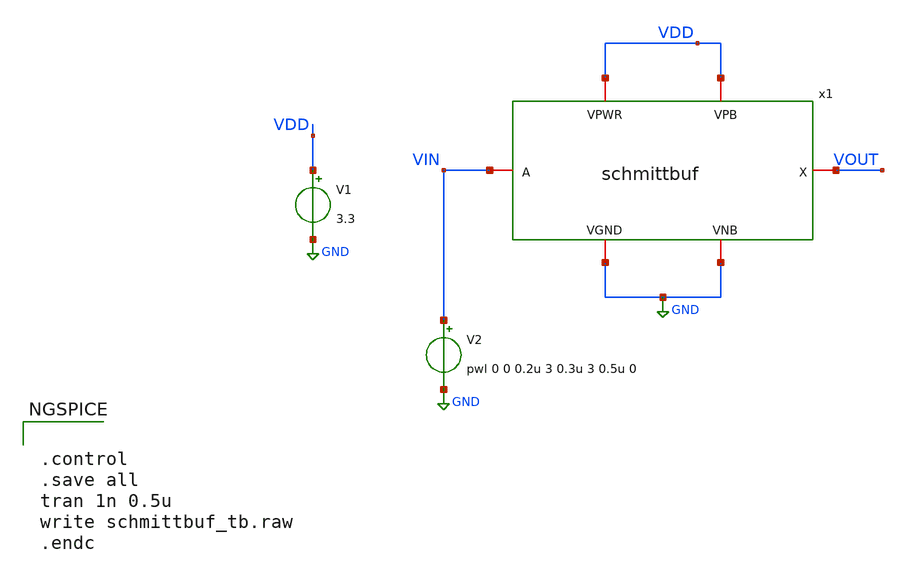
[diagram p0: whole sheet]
** sch_path: images/iic-osic-tools/addons/examples/open-pmic/design/oscillator/schmittbuf_tb.sch
**.subckt schmittbuf_tb
x1 VDD GND VDD GND VIN VOUT schmittbuf
V1 VDD GND 3.3
V2 VIN GND pwl 0 0 0.2u 3 0.3u 3 0.5u 0
**** begin user architecture code

.include $::SKYWATER_MODELS/cells/nfet_01v8/sky130_fd_pr__nfet_01v8__tt.corner.spice
.include $::SKYWATER_MODELS/cells/nfet_01v8_lvt/sky130_fd_pr__nfet_01v8_lvt__tt.corner.spice
.include $::SKYWATER_MODELS/cells/pfet_01v8/sky130_fd_pr__pfet_01v8__tt.corner.spice
.include $::SKYWATER_MODELS/cells/nfet_03v3_nvt/sky130_fd_pr__nfet_03v3_nvt__tt.corner.spice
.include $::SKYWATER_MODELS/cells/nfet_05v0_nvt/sky130_fd_pr__nfet_05v0_nvt__tt.corner.spice
.include $::SKYWATER_MODELS/cells/esd_nfet_01v8/sky130_fd_pr__esd_nfet_01v8__tt.corner.spice
.include $::SKYWATER_MODELS/cells/pfet_01v8_lvt/sky130_fd_pr__pfet_01v8_lvt__tt.corner.spice
.include $::SKYWATER_MODELS/cells/pfet_01v8_hvt/sky130_fd_pr__pfet_01v8_hvt__tt.corner.spice
.include $::SKYWATER_MODELS/cells/esd_pfet_g5v0d10v5/sky130_fd_pr__esd_pfet_g5v0d10v5__tt.corner.spice
.include $::SKYWATER_MODELS/cells/pfet_g5v0d10v5/sky130_fd_pr__pfet_g5v0d10v5__tt.corner.spice
.include $::SKYWATER_MODELS/cells/pfet_g5v0d16v0/sky130_fd_pr__pfet_g5v0d16v0__tt.corner.spice
.include $::SKYWATER_MODELS/cells/nfet_g5v0d10v5/sky130_fd_pr__nfet_g5v0d10v5__tt.corner.spice
.include $::SKYWATER_MODELS/cells/nfet_g5v0d16v0/sky130_fd_pr__nfet_g5v0d16v0__tt_discrete.corner.spice
.include $::SKYWATER_MODELS/cells/esd_nfet_g5v0d10v5/sky130_fd_pr__esd_nfet_g5v0d10v5__tt.corner.spice
.include $::SKYWATER_MODELS/models/corners/tt/nonfet.spice
* Mismatch parameters
.include $::SKYWATER_MODELS/cells/nfet_01v8/sky130_fd_pr__nfet_01v8__mismatch.corner.spice
.include $::SKYWATER_MODELS/cells/pfet_01v8/sky130_fd_pr__pfet_01v8__mismatch.corner.spice
.include $::SKYWATER_MODELS/cells/nfet_01v8_lvt/sky130_fd_pr__nfet_01v8_lvt__mismatch.corner.spice
.include $::SKYWATER_MODELS/cells/pfet_01v8_lvt/sky130_fd_pr__pfet_01v8_lvt__mismatch.corner.spice
.include $::SKYWATER_MODELS/cells/pfet_01v8_hvt/sky130_fd_pr__pfet_01v8_hvt__mismatch.corner.spice
.include $::SKYWATER_MODELS/cells/nfet_g5v0d10v5/sky130_fd_pr__nfet_g5v0d10v5__mismatch.corner.spice
.include $::SKYWATER_MODELS/cells/pfet_g5v0d10v5/sky130_fd_pr__pfet_g5v0d10v5__mismatch.corner.spice
.include $::SKYWATER_MODELS/cells/nfet_05v0_nvt/sky130_fd_pr__nfet_05v0_nvt__mismatch.corner.spice
.include $::SKYWATER_MODELS/cells/nfet_03v3_nvt/sky130_fd_pr__nfet_03v3_nvt__mismatch.corner.spice
* Resistor$::SKYWATER_MODELS/Capacitor
.include $::SKYWATER_MODELS/models/r+c/res_typical__cap_typical.spice
.include $::SKYWATER_MODELS/models/r+c/res_typical__cap_typical__lin.spice
* Special cells
.include $::SKYWATER_MODELS/models/corners/tt/specialized_cells.spice
* All models
.include $::SKYWATER_MODELS/models/all.spice
* Corner
.include $::SKYWATER_MODELS/models/corners/tt/rf.spice



.control
.save all
tran 1n 0.5u
write schmittbuf_tb.raw
.endc


**** end user architecture code
**.ends

* expanding   symbol:  design/oscillator/schmittbuf.sym # of pins=6
** sym_path: images/iic-osic-tools/addons/examples/open-pmic/design/oscillator/schmittbuf.sym
** sch_path: images/iic-osic-tools/addons/examples/open-pmic/design/oscillator/schmittbuf.sch
.subckt schmittbuf VPWR VGND VPB VNB A X
*.iopin VPWR
*.iopin VGND
*.iopin VPB
*.iopin VNB
*.iopin A
*.iopin X
XM1 net1 A net2 VNB sky130_fd_pr__nfet_g5v0d10v5 L=1 W=5 nf=1 ad='int((nf+1)/2) * W/nf * 0.29' as='int((nf+2)/2) * W/nf * 0.29'
+ pd='2*int((nf+1)/2) * (W/nf + 0.29)' ps='2*int((nf+2)/2) * (W/nf + 0.29)' nrd='0.29 / W' nrs='0.29 / W'
+ sa=0 sb=0 sd=0 mult=2 m=2
XM8 net2 A VGND VNB sky130_fd_pr__nfet_g5v0d10v5 L=1 W=5 nf=1 ad='int((nf+1)/2) * W/nf * 0.29' as='int((nf+2)/2) * W/nf * 0.29'
+ pd='2*int((nf+1)/2) * (W/nf + 0.29)' ps='2*int((nf+2)/2) * (W/nf + 0.29)' nrd='0.29 / W' nrs='0.29 / W'
+ sa=0 sb=0 sd=0 mult=2 m=2
XM0 net1 A net3 VPB sky130_fd_pr__pfet_g5v0d10v5 L=1 W=5 nf=1 ad='int((nf+1)/2) * W/nf * 0.29' as='int((nf+2)/2) * W/nf * 0.29'
+ pd='2*int((nf+1)/2) * (W/nf + 0.29)' ps='2*int((nf+2)/2) * (W/nf + 0.29)' nrd='0.29 / W' nrs='0.29 / W'
+ sa=0 sb=0 sd=0 mult=4 m=4
XM4 net3 A VPWR VPB sky130_fd_pr__pfet_g5v0d10v5 L=1 W=5 nf=1 ad='int((nf+1)/2) * W/nf * 0.29' as='int((nf+2)/2) * W/nf * 0.29'
+ pd='2*int((nf+1)/2) * (W/nf + 0.29)' ps='2*int((nf+2)/2) * (W/nf + 0.29)' nrd='0.29 / W' nrs='0.29 / W'
+ sa=0 sb=0 sd=0 mult=4 m=4
XM7 VPWR net1 X VPB sky130_fd_pr__pfet_g5v0d10v5 L=1 W=5 nf=1 ad='int((nf+1)/2) * W/nf * 0.29' as='int((nf+2)/2) * W/nf * 0.29'
+ pd='2*int((nf+1)/2) * (W/nf + 0.29)' ps='2*int((nf+2)/2) * (W/nf + 0.29)' nrd='0.29 / W' nrs='0.29 / W'
+ sa=0 sb=0 sd=0 mult=4 m=4
XM6 VGND net1 X VNB sky130_fd_pr__nfet_g5v0d10v5 L=1 W=5 nf=1 ad='int((nf+1)/2) * W/nf * 0.29' as='int((nf+2)/2) * W/nf * 0.29'
+ pd='2*int((nf+1)/2) * (W/nf + 0.29)' ps='2*int((nf+2)/2) * (W/nf + 0.29)' nrd='0.29 / W' nrs='0.29 / W'
+ sa=0 sb=0 sd=0 mult=2 m=2
XM9 net4 net1 net3 VPB sky130_fd_pr__pfet_g5v0d10v5 L=0.5 W=5 nf=1 ad='int((nf+1)/2) * W/nf * 0.29' as='int((nf+2)/2) * W/nf * 0.29'
+ pd='2*int((nf+1)/2) * (W/nf + 0.29)' ps='2*int((nf+2)/2) * (W/nf + 0.29)' nrd='0.29 / W' nrs='0.29 / W'
+ sa=0 sb=0 sd=0 mult=8 m=8
XM5 net5 net1 net2 VNB sky130_fd_pr__nfet_g5v0d10v5 L=0.5 W=5 nf=1 ad='int((nf+1)/2) * W/nf * 0.29' as='int((nf+2)/2) * W/nf * 0.29'
+ pd='2*int((nf+1)/2) * (W/nf + 0.29)' ps='2*int((nf+2)/2) * (W/nf + 0.29)' nrd='0.29 / W' nrs='0.29 / W'
+ sa=0 sb=0 sd=0 mult=4 m=4
XR1 VGND net4 VNB sky130_fd_pr__res_generic_nd W=2 L=6 mult=1 m=1
XR2 net5 VPWR VPB sky130_fd_pr__res_generic_pd W=2 L=12 mult=1 m=1
.ends

.GLOBAL GND
**** begin user architecture code
[sky130_models]
**** end user architecture code
.end
